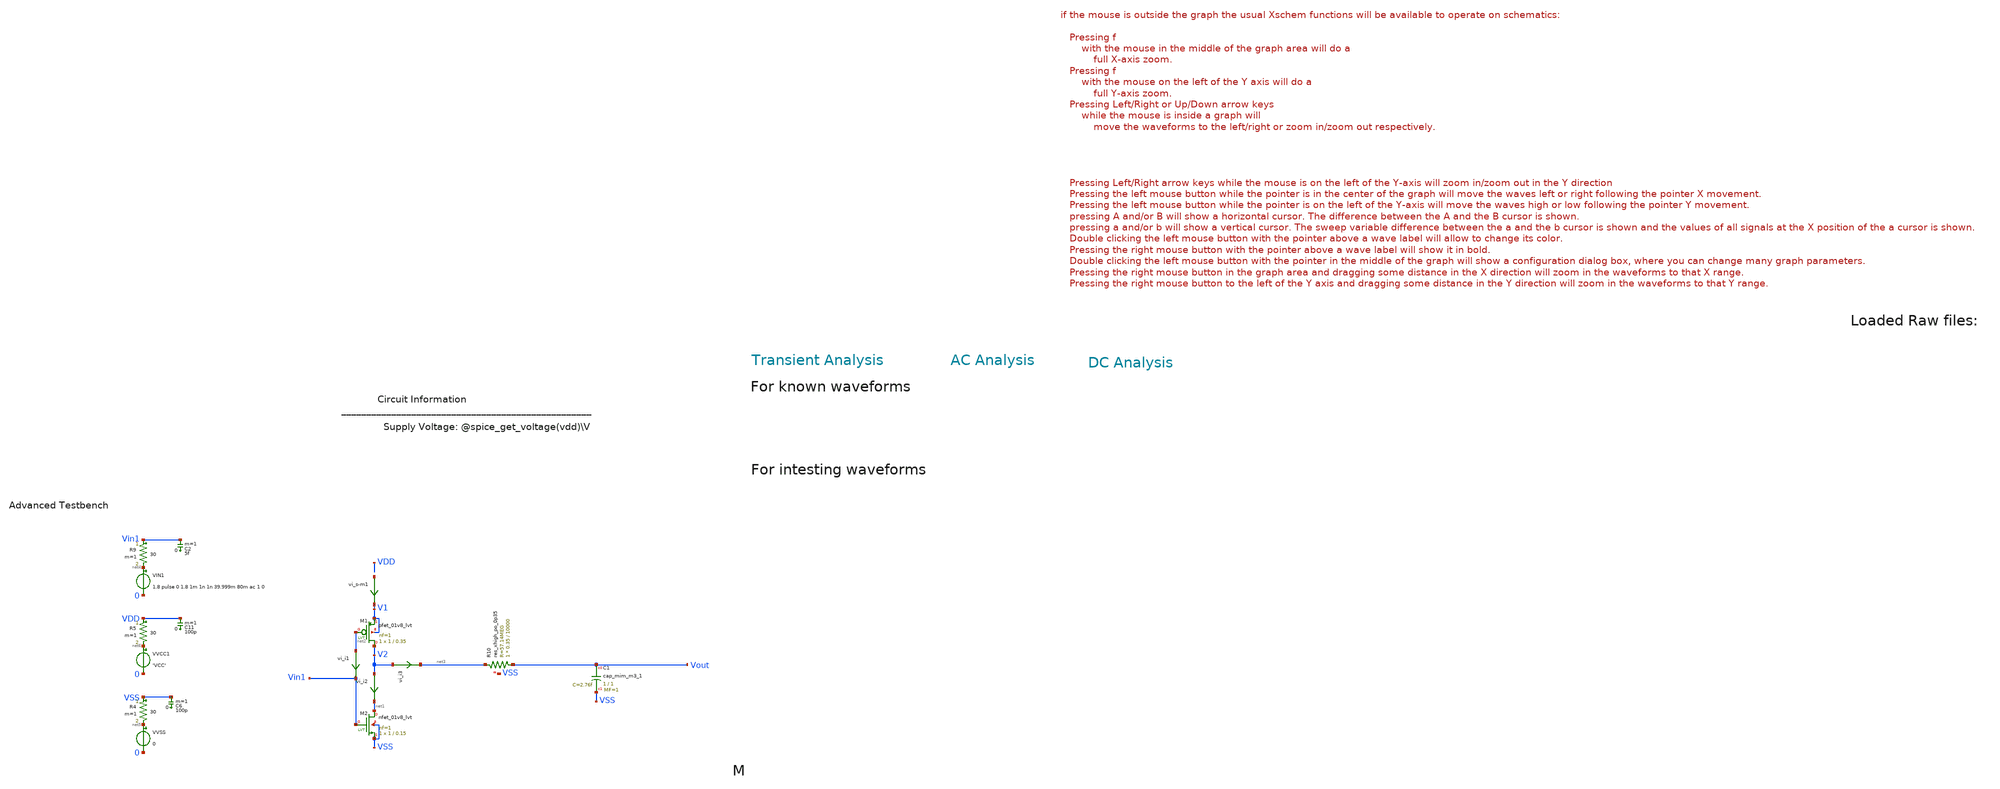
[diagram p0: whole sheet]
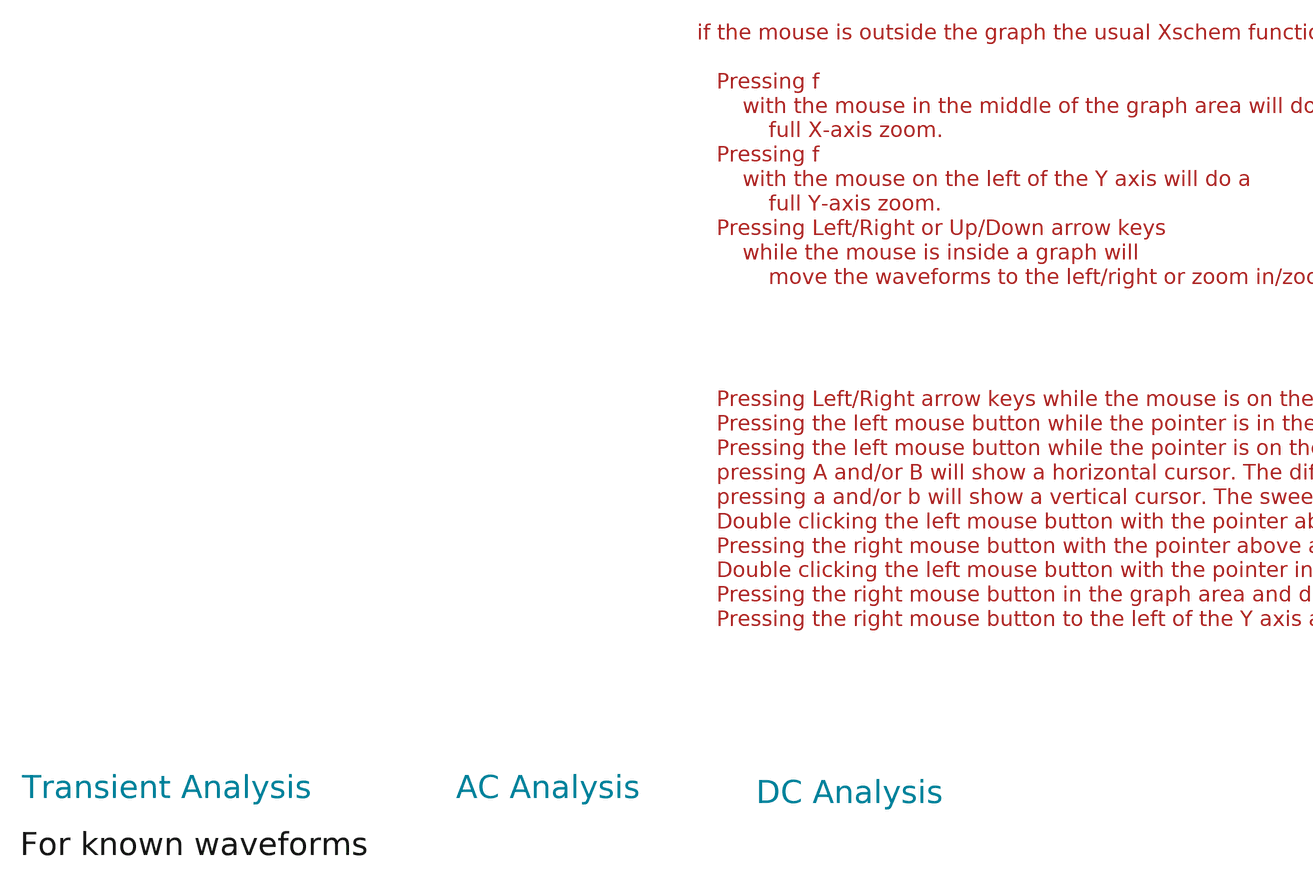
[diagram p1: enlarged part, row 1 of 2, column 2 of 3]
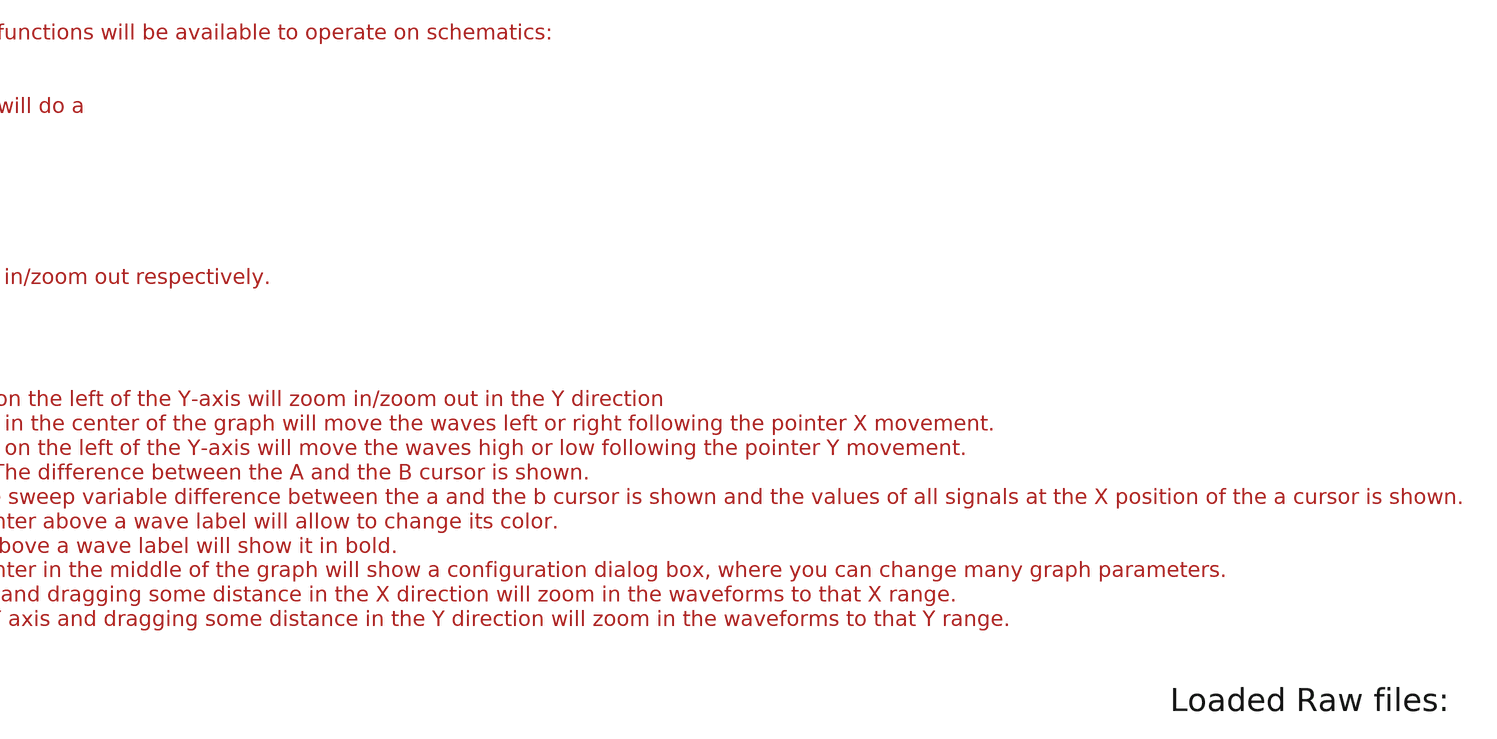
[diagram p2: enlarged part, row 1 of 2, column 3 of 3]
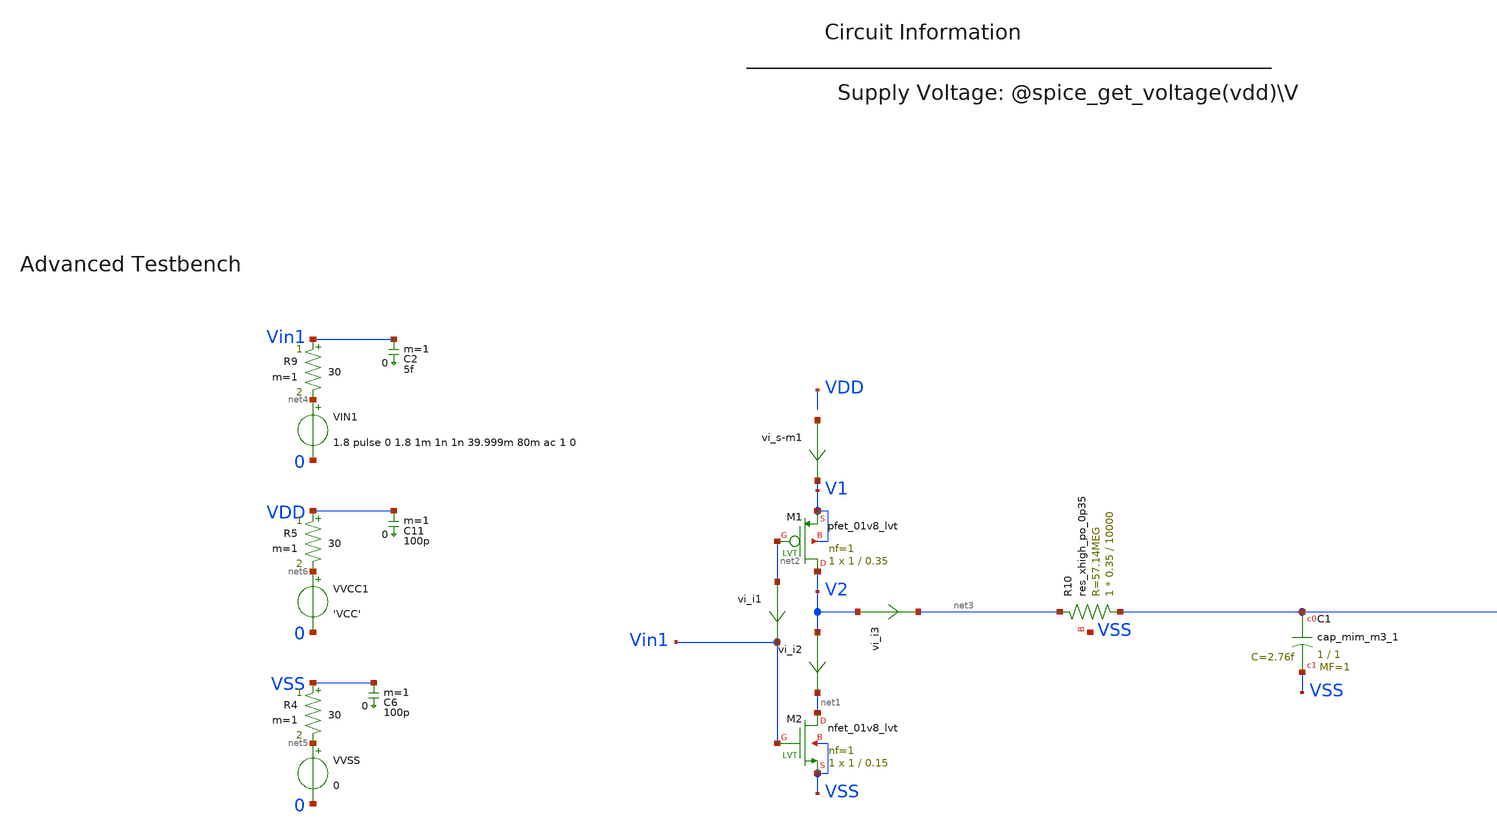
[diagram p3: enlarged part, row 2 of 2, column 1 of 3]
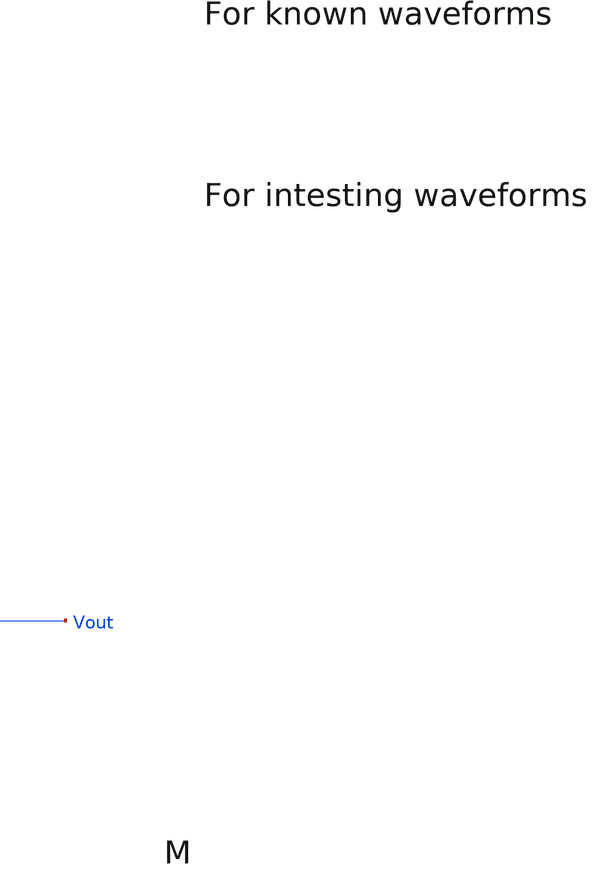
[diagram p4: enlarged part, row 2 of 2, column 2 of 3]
** sch_path: tt10-hdl/tt_um_test_commit/xschem/A1_templates/testbench_template.sch
* Copyright (C) 1998-2024 Stefan Frederik Schippers
* This program is free software; you can redistribute it and/or modify
* it under the terms of the GNU General Public License as published by
* the Free Software Foundation; either version 2 of the License, or
* (at your option) any later version.
* This program is distributed in the hope that it will be useful,
* but WITHOUT ANY WARRANTY; without even the implied warranty of
* MERCHANTABILITY or FITNESS FOR A PARTICULAR PURPOSE.  See the
* GNU General Public License for more details.
* You should have received a copy of the GNU General Public License
* along with this program; if not, write to the Free Software
**.subckt testbench_template
vi_i2 V2 net1 0
.save i(vi_i2)
XM1 V2 net2 V1 V1 sky130_fd_pr__pfet_01v8_lvt L=0.35 W=1 nf=1 ad='int((1 + 1)/2) * 1 / 1 * 0.29' as='int((1 + 2)/2) * 1 / 1 * 0.29'
+ pd='2*int((1 + 1)/2) * (1 / 1 + 0.29)' ps='2*int((1 + 2)/2) * (1 / 1 + 0.29)' nrd='0.29 / 1 ' nrs='0.29 / 1 '
+ sa=0 sb=0 sd=0 mult=1 m=1
XM2 net1 Vin1 VSS VSS sky130_fd_pr__nfet_01v8_lvt L=0.15 W=1 nf=1 ad='int((1 + 1)/2) * 1 / 1 * 0.29'
+ as='int((1 + 2)/2) * 1 / 1 * 0.29' pd='2*int((1 + 1)/2) * (1 / 1 + 0.29)' ps='2*int((1 + 2)/2) * (1 / 1 + 0.29)'
+ nrd='0.29 / 1 ' nrs='0.29 / 1 ' sa=0 sb=0 sd=0 mult=1 m=1
XC1 Vout VSS sky130_fd_pr__cap_mim_m3_1 W=1 L=1 MF=1 m=1
vi_i1 net2 Vin1 0
.save i(vi_i1)
vi_i3 V2 net3 0
.save i(vi_i3)
XR10 Vout net3 VSS sky130_fd_pr__res_xhigh_po_0p35 L=10000 mult=1 m=1
VIN1 net4 0 1.8 pulse 0 1.8 1m 1n 1n 39.999m 80m ac 1 0
VVSS net5 0 0
R4 VSS net5 30 m=1
C6 VSS 0 100p m=1
VVCC1 net6 0 'VCC'
R5 VDD net6 30 m=1
C11 VDD 0 100p m=1
R9 Vin1 net4 30 m=1
C2 Vin1 0 5f m=1
vi_s-m1 net7 V1 0
.save i(vi_s-m1)
**** begin user architecture code



.temp 30
*.param IB=1n
.param VCC = 1.8

.option savecurrents
.save all @m1[gm]
.control
  save all alli
  op
  let power=-v(vcc) * i(vvcc)
  settype power power
  write template_adv_tb.raw
  set appendwrite

  *dc vin1 0 1.8 0.001
  *write template_adv_tb.raw

  tran 1u 2m
  *tran 0.01n 15n
  write template_adv_tb.raw

  *ac dec 10 1 1G
  *remzerovec
  *write template_adv_tb.raw



  quit 0




.endc





** opencircuitdesign pdks install
.lib $::SKYWATER_MODELS/sky130.lib.spice tt
.include $::SKYWATER_STDCELLS/sky130_fd_sc_hd.spice


**** end user architecture code
**.ends
.end
